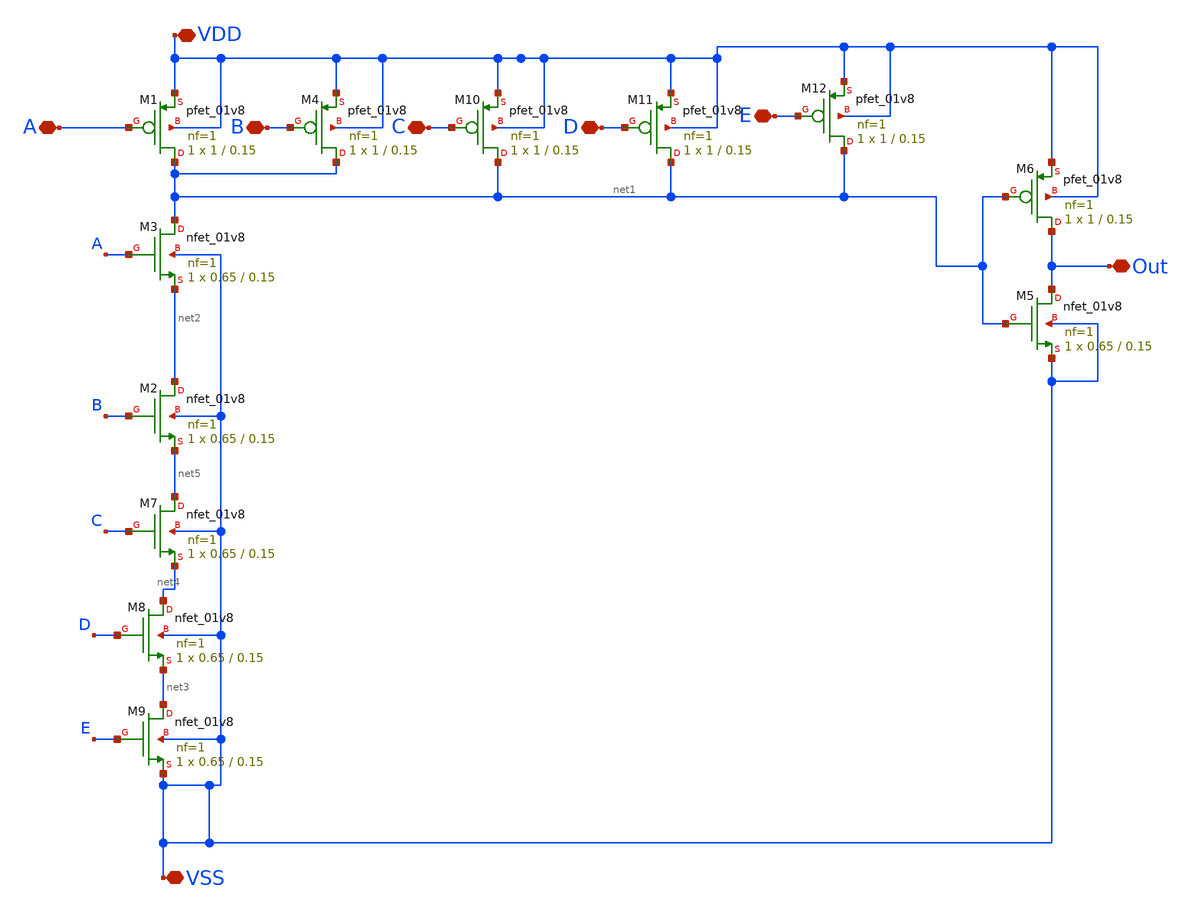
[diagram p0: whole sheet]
** sch_path: MUX/AND.sch
**.subckt AND VDD A VSS B Out C D E
*.iopin VDD
*.iopin A
*.iopin VSS
*.iopin B
*.iopin Out
*.iopin C
*.iopin D
*.iopin E
XM3 net1 A net2 VSS sky130_fd_pr__nfet_01v8 L=0.15 W=0.65 nf=1 ad='int((nf+1)/2) * W/nf * 0.29' as='int((nf+2)/2) * W/nf * 0.29'
+ pd='2*int((nf+1)/2) * (W/nf + 0.29)' ps='2*int((nf+2)/2) * (W/nf + 0.29)' nrd='0.29 / W' nrs='0.29 / W'
+ sa=0 sb=0 sd=0 mult=1 m=1
XM1 net1 A VDD VDD sky130_fd_pr__pfet_01v8 L=0.15 W=1 nf=1 ad='int((nf+1)/2) * W/nf * 0.29' as='int((nf+2)/2) * W/nf * 0.29'
+ pd='2*int((nf+1)/2) * (W/nf + 0.29)' ps='2*int((nf+2)/2) * (W/nf + 0.29)' nrd='0.29 / W' nrs='0.29 / W'
+ sa=0 sb=0 sd=0 mult=1 m=1
XM5 Out net1 VSS VSS sky130_fd_pr__nfet_01v8 L=0.15 W=0.65 nf=1 ad='int((nf+1)/2) * W/nf * 0.29' as='int((nf+2)/2) * W/nf * 0.29'
+ pd='2*int((nf+1)/2) * (W/nf + 0.29)' ps='2*int((nf+2)/2) * (W/nf + 0.29)' nrd='0.29 / W' nrs='0.29 / W'
+ sa=0 sb=0 sd=0 mult=1 m=1
XM6 Out net1 VDD VDD sky130_fd_pr__pfet_01v8 L=0.15 W=1 nf=1 ad='int((nf+1)/2) * W/nf * 0.29' as='int((nf+2)/2) * W/nf * 0.29'
+ pd='2*int((nf+1)/2) * (W/nf + 0.29)' ps='2*int((nf+2)/2) * (W/nf + 0.29)' nrd='0.29 / W' nrs='0.29 / W'
+ sa=0 sb=0 sd=0 mult=1 m=1
XM4 net1 B VDD VDD sky130_fd_pr__pfet_01v8 L=0.15 W=1 nf=1 ad='int((nf+1)/2) * W/nf * 0.29' as='int((nf+2)/2) * W/nf * 0.29'
+ pd='2*int((nf+1)/2) * (W/nf + 0.29)' ps='2*int((nf+2)/2) * (W/nf + 0.29)' nrd='0.29 / W' nrs='0.29 / W'
+ sa=0 sb=0 sd=0 mult=1 m=1
XM10 net1 C VDD VDD sky130_fd_pr__pfet_01v8 L=0.15 W=1 nf=1 ad='int((nf+1)/2) * W/nf * 0.29' as='int((nf+2)/2) * W/nf * 0.29'
+ pd='2*int((nf+1)/2) * (W/nf + 0.29)' ps='2*int((nf+2)/2) * (W/nf + 0.29)' nrd='0.29 / W' nrs='0.29 / W'
+ sa=0 sb=0 sd=0 mult=1 m=1
XM11 net1 D VDD VDD sky130_fd_pr__pfet_01v8 L=0.15 W=1 nf=1 ad='int((nf+1)/2) * W/nf * 0.29' as='int((nf+2)/2) * W/nf * 0.29'
+ pd='2*int((nf+1)/2) * (W/nf + 0.29)' ps='2*int((nf+2)/2) * (W/nf + 0.29)' nrd='0.29 / W' nrs='0.29 / W'
+ sa=0 sb=0 sd=0 mult=1 m=1
XM12 net1 E VDD VDD sky130_fd_pr__pfet_01v8 L=0.15 W=1 nf=1 ad='int((nf+1)/2) * W/nf * 0.29' as='int((nf+2)/2) * W/nf * 0.29'
+ pd='2*int((nf+1)/2) * (W/nf + 0.29)' ps='2*int((nf+2)/2) * (W/nf + 0.29)' nrd='0.29 / W' nrs='0.29 / W'
+ sa=0 sb=0 sd=0 mult=1 m=1
XM2 net2 B net5 VSS sky130_fd_pr__nfet_01v8 L=0.15 W=0.65 nf=1 ad='int((nf+1)/2) * W/nf * 0.29' as='int((nf+2)/2) * W/nf * 0.29'
+ pd='2*int((nf+1)/2) * (W/nf + 0.29)' ps='2*int((nf+2)/2) * (W/nf + 0.29)' nrd='0.29 / W' nrs='0.29 / W'
+ sa=0 sb=0 sd=0 mult=1 m=1
XM7 net5 C net4 VSS sky130_fd_pr__nfet_01v8 L=0.15 W=0.65 nf=1 ad='int((nf+1)/2) * W/nf * 0.29' as='int((nf+2)/2) * W/nf * 0.29'
+ pd='2*int((nf+1)/2) * (W/nf + 0.29)' ps='2*int((nf+2)/2) * (W/nf + 0.29)' nrd='0.29 / W' nrs='0.29 / W'
+ sa=0 sb=0 sd=0 mult=1 m=1
XM8 net4 D net3 VSS sky130_fd_pr__nfet_01v8 L=0.15 W=0.65 nf=1 ad='int((nf+1)/2) * W/nf * 0.29' as='int((nf+2)/2) * W/nf * 0.29'
+ pd='2*int((nf+1)/2) * (W/nf + 0.29)' ps='2*int((nf+2)/2) * (W/nf + 0.29)' nrd='0.29 / W' nrs='0.29 / W'
+ sa=0 sb=0 sd=0 mult=1 m=1
XM9 net3 E VSS VSS sky130_fd_pr__nfet_01v8 L=0.15 W=0.65 nf=1 ad='int((nf+1)/2) * W/nf * 0.29' as='int((nf+2)/2) * W/nf * 0.29'
+ pd='2*int((nf+1)/2) * (W/nf + 0.29)' ps='2*int((nf+2)/2) * (W/nf + 0.29)' nrd='0.29 / W' nrs='0.29 / W'
+ sa=0 sb=0 sd=0 mult=1 m=1
**.ends
.end
